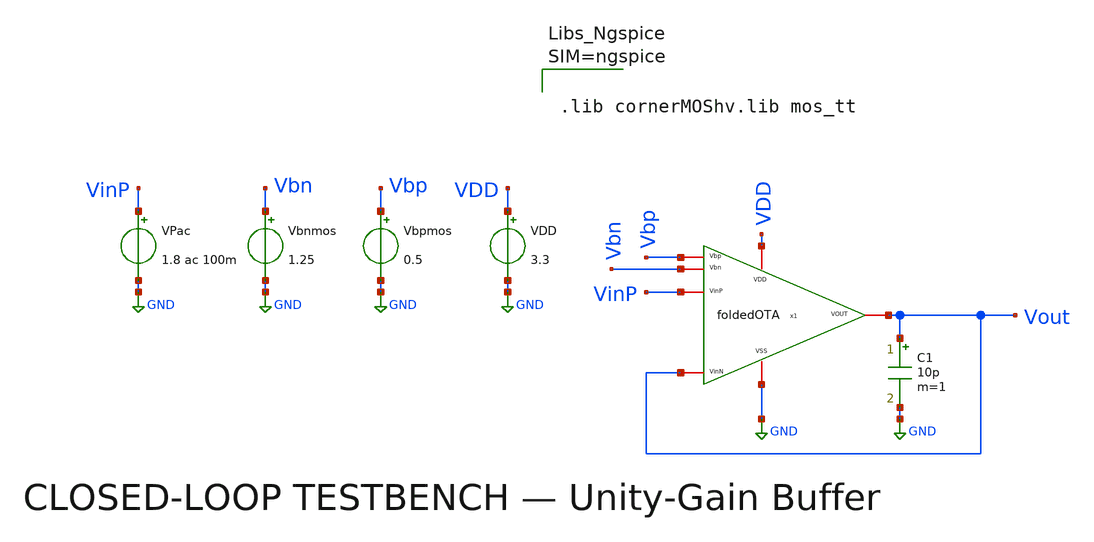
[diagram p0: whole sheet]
** sch_path: closedloop/CL-foldedOTA.sch
* v1_ideal_current_sources/schematic/foldedOTA.sch:
* (c) 2026 Fares Satouh
**.subckt CL-foldedOTA
VPac VinP GND 1.8 ac 100m
Vbnmos Vbn GND 1.25
Vbpmos Vbp GND 0.5
VDD VDD GND 3.3
x1 VDD Vbp Vout VinP Vout Vbn GND foldedOTA
C1 Vout GND 10p m=1
**** begin user architecture code



.lib cornerMOShv.lib mos_tt





.control
destroy all
ac dec 20 1 900Meg
run

let gain_db    = db(Vout/VinP)
let gain_phase = phase(Vout/VinP)*180/PI

save all

meas ac dc_gain_cl find gain_db at=1
meas ac f3db_cl    when gain_db='dc_gain_cl-3'
meas ac gpeak      max  gain_db

plot gain_db    ylabel 'Gain (dB)'   xlog title 'Closed-Loop Gain'
plot gain_phase ylabel 'Phase (deg)' xlog title 'Closed-Loop Phase'

echo
echo '================ CLOSED-LOOP AC SUMMARY ================'
print dc_gain_cl
print f3db_cl
print gpeak
echo '=========================================================='

.endc


**** end user architecture code
**.ends

* expanding   symbol:  foldedOTA.sym # of pins=7
** sym_path: v1_ideal_current_sources/schematic/foldedOTA.sym
** sch_path: v1_ideal_current_sources/schematic/foldedOTA.sch
.subckt foldedOTA VDD Vbp VOUT VinP VinN Vbn VSS
*.iopin VDD
*.iopin VSS
*.iopin VOUT
*.iopin Vbp
*.iopin Vbn
*.iopin VinN
*.iopin VinP
XM1 net2 VinP net1 VSS sg13_hv_nmos w=28u l=1u ng=4 m=1 mm_ok=1
XM2 net3 VinN net1 VSS sg13_hv_nmos w=28u l=1u ng=4 m=1 mm_ok=1
XM3 net1 net8 VSS VSS sg13_hv_nmos w=15u l=1u ng=3 m=1 mm_ok=1
XM4 net2 net7 VDD VDD sg13_hv_pmos w=14u l=1u ng=2 m=1 mm_ok=1
XM5 net3 net7 VDD VDD sg13_hv_pmos w=14u l=1u ng=2 m=1 mm_ok=1
XM6 net4 Vbp net2 VDD sg13_hv_pmos w=2u l=1u ng=1 m=1 mm_ok=1
XM7 VOUT Vbp net3 VDD sg13_hv_pmos w=2u l=1u ng=1 m=1 mm_ok=1
XM8 net4 Vbn net5 VSS sg13_hv_nmos w=7u l=1u ng=1 m=1 mm_ok=1
XM9 VOUT Vbn net6 VSS sg13_hv_nmos w=7u l=1u ng=1 m=1 mm_ok=1
XM10 net5 net4 VSS VSS sg13_hv_nmos w=7u l=1u ng=1 m=1 mm_ok=1
XM11 net6 net4 VSS VSS sg13_hv_nmos w=7u l=1u ng=1 m=1 mm_ok=1
XM12 net8 net8 VSS VSS sg13_hv_nmos w=15u l=1u ng=3 m=1 mm_ok=1
I0 VDD net8 50u
XM13 net7 net7 VDD VDD sg13_hv_pmos w=14u l=1u ng=2 m=1 mm_ok=1
I1 net7 VSS 50u
.ends

.GLOBAL GND
.end
